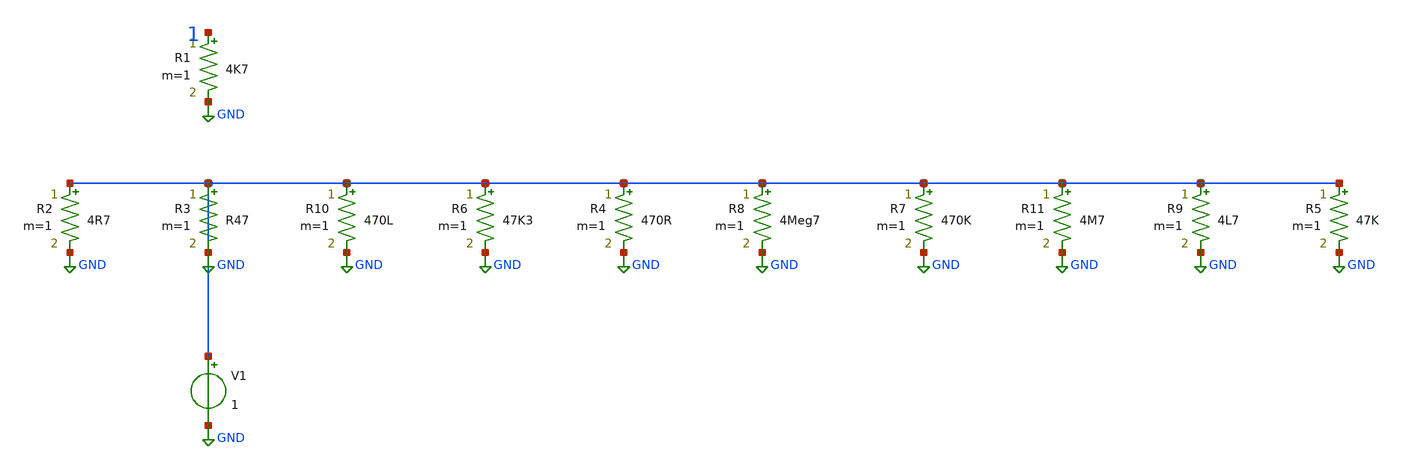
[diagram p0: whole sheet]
** sch_path: data/sch/aicas_RKM-R-1.sch
**.subckt aicas_RKM-R-1
V1 GND GND 1
R1 1 GND 4K7 m=1
R2 GND GND 4R7 m=1
R3 GND GND R47 m=1
R4 GND GND 470R m=1
R5 GND GND 47K m=1
R6 GND GND 47K3 m=1
R7 GND GND 470K m=1
R8 GND GND 4Meg7 m=1
R9 GND GND 4L7 m=1
R10 GND GND 470L m=1
R11 GND GND 4M7 m=1
**.ends
.GLOBAL GND
.end
